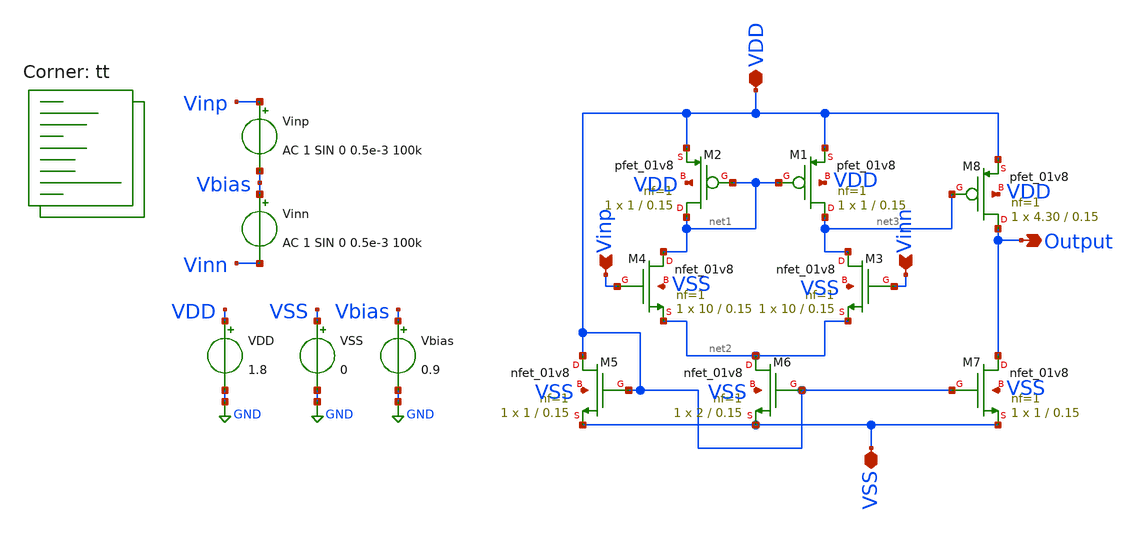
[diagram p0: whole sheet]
** sch_path: xschem/src/hw02.sch
**.subckt hw02 Output Vinp Vinn VDD VSS
*.opin Output
*.ipin Vinp
*.ipin Vinn
*.iopin VDD
*.iopin VSS
XM2 net1 net1 VDD VDD sky130_fd_pr__pfet_01v8 L=0.15 W=1 nf=1 ad='int((nf+1)/2) * W/nf * 0.29' as='int((nf+2)/2) * W/nf * 0.29'
+ pd='2*int((nf+1)/2) * (W/nf + 0.29)' ps='2*int((nf+2)/2) * (W/nf + 0.29)' nrd='0.29 / W' nrs='0.29 / W'
+ sa=0 sb=0 sd=0 mult=1 m=1
XM1 net3 net1 VDD VDD sky130_fd_pr__pfet_01v8 L=0.15 W=1 nf=1 ad='int((nf+1)/2) * W/nf * 0.29' as='int((nf+2)/2) * W/nf * 0.29'
+ pd='2*int((nf+1)/2) * (W/nf + 0.29)' ps='2*int((nf+2)/2) * (W/nf + 0.29)' nrd='0.29 / W' nrs='0.29 / W'
+ sa=0 sb=0 sd=0 mult=1 m=1
XM3 net3 Vinn net2 VSS sky130_fd_pr__nfet_01v8 L=0.15 W=10 nf=1 ad='int((nf+1)/2) * W/nf * 0.29' as='int((nf+2)/2) * W/nf * 0.29'
+ pd='2*int((nf+1)/2) * (W/nf + 0.29)' ps='2*int((nf+2)/2) * (W/nf + 0.29)' nrd='0.29 / W' nrs='0.29 / W'
+ sa=0 sb=0 sd=0 mult=1 m=1
XM4 net1 Vinp net2 VSS sky130_fd_pr__nfet_01v8 L=0.15 W=10 nf=1 ad='int((nf+1)/2) * W/nf * 0.29' as='int((nf+2)/2) * W/nf * 0.29'
+ pd='2*int((nf+1)/2) * (W/nf + 0.29)' ps='2*int((nf+2)/2) * (W/nf + 0.29)' nrd='0.29 / W' nrs='0.29 / W'
+ sa=0 sb=0 sd=0 mult=1 m=1
XM5 VDD VDD VSS VSS sky130_fd_pr__nfet_01v8 L=0.15 W=1 nf=1 ad='int((nf+1)/2) * W/nf * 0.29' as='int((nf+2)/2) * W/nf * 0.29'
+ pd='2*int((nf+1)/2) * (W/nf + 0.29)' ps='2*int((nf+2)/2) * (W/nf + 0.29)' nrd='0.29 / W' nrs='0.29 / W'
+ sa=0 sb=0 sd=0 mult=1 m=1
XM6 net2 VDD VSS VSS sky130_fd_pr__nfet_01v8 L=0.15 W=2 nf=1 ad='int((nf+1)/2) * W/nf * 0.29' as='int((nf+2)/2) * W/nf * 0.29'
+ pd='2*int((nf+1)/2) * (W/nf + 0.29)' ps='2*int((nf+2)/2) * (W/nf + 0.29)' nrd='0.29 / W' nrs='0.29 / W'
+ sa=0 sb=0 sd=0 mult=1 m=1
XM7 Output VDD VSS VSS sky130_fd_pr__nfet_01v8 L=0.15 W=1 nf=1 ad='int((nf+1)/2) * W/nf * 0.29' as='int((nf+2)/2) * W/nf * 0.29'
+ pd='2*int((nf+1)/2) * (W/nf + 0.29)' ps='2*int((nf+2)/2) * (W/nf + 0.29)' nrd='0.29 / W' nrs='0.29 / W'
+ sa=0 sb=0 sd=0 mult=1 m=1
XM8 Output net3 VDD VDD sky130_fd_pr__pfet_01v8 L=0.15 W=4.30 nf=1 ad='int((nf+1)/2) * W/nf * 0.29' as='int((nf+2)/2) * W/nf * 0.29'
+ pd='2*int((nf+1)/2) * (W/nf + 0.29)' ps='2*int((nf+2)/2) * (W/nf + 0.29)' nrd='0.29 / W' nrs='0.29 / W'
+ sa=0 sb=0 sd=0 mult=1 m=1
VDD VDD GND 1.8
VSS VSS GND 0
Vbias Vbias GND 0.9
Vinp Vinp Vbias AC 1 SIN 0 0.5e-3 100k
Vinn Vbias Vinn AC 1 SIN 0 0.5e-3 100k
**** begin user architecture code
.lib $::SKYWATER_MODELS/sky130.lib.spice tt



* ngspice commands
.options list act
.options method=gear
.temp 25

.control
save all
ac dec 10 1 3e9
plot dB(Output)
tran 1n 50u
plot Output
write final_test.raw
.endc



**** end user architecture code
**.ends
.GLOBAL GND
.end
